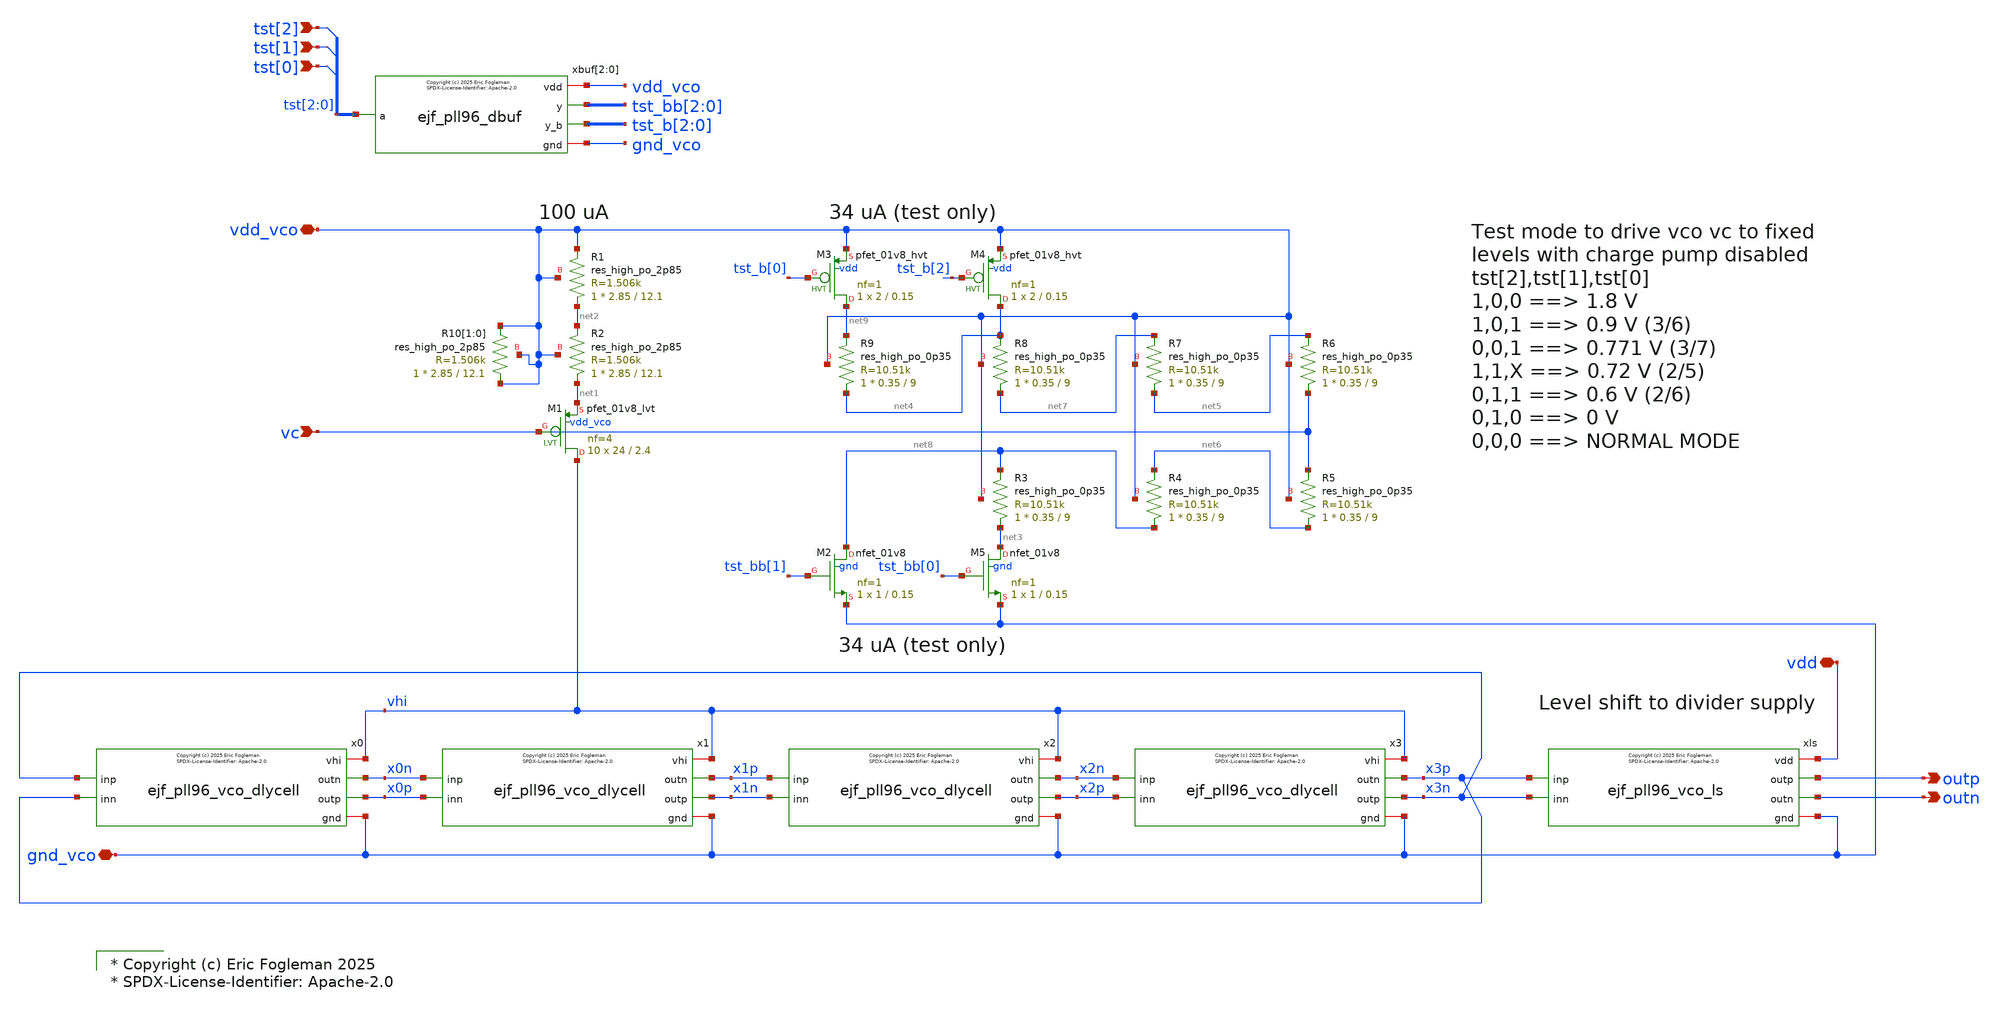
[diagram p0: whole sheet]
** sch_path: xschem/ejf_pll96_vco.sch
* xschem/ejf_pll96_dbuf.sym:
* Copyright (c) 2025 Eric Fogleman

* Copyright (c) Eric Fogleman 2025
* SPDX-License-Identifier: Apache-2.0

**.subckt ejf_pll96_vco vc vdd_vco outp gnd_vco vdd outn tst[2] tst[1] tst[0]
*.ipin vc
*.iopin vdd_vco
*.opin outp
*.iopin gnd_vco
*.iopin vdd
*.opin outn
*.ipin tst[2]
*.ipin tst[1]
*.ipin tst[0]
x1 vhi x1p x1n x0n x0p gnd_vco ejf_pll96_vco_dlycell
x2 vhi x2n x2p x1p x1n gnd_vco ejf_pll96_vco_dlycell
x0 vhi x0n x0p x3n x3p gnd_vco ejf_pll96_vco_dlycell
x3 vhi x3p x3n x2n x2p gnd_vco ejf_pll96_vco_dlycell
xls vdd x3p outp outn x3n gnd_vco ejf_pll96_vco_ls
XM1 vhi vc net1 vdd_vco sky130_fd_pr__pfet_01v8_lvt L=2.4 W=24 nf=4 ad='int((nf+1)/2) * W/nf * 0.29'
+ as='int((nf+2)/2) * W/nf * 0.29' pd='2*int((nf+1)/2) * (W/nf + 0.29)' ps='2*int((nf+2)/2) * (W/nf + 0.29)'
+ nrd='0.29 / W' nrs='0.29 / W' sa=0 sb=0 sd=0 mult=10 m=10
XR1 net2 vdd_vco vdd_vco sky130_fd_pr__res_high_po_2p85 L=12.1 mult=1 m=1
XR2 net1 net2 vdd_vco sky130_fd_pr__res_high_po_2p85 L=12.1 mult=1 m=1
XR10[1] vdd_vco vdd_vco vdd_vco sky130_fd_pr__res_high_po_2p85 L=12.1 mult=1 m=1
XR10[0] vdd_vco vdd_vco vdd_vco sky130_fd_pr__res_high_po_2p85 L=12.1 mult=1 m=1
XM2 net8 tst_bb[1] gnd_vco gnd sky130_fd_pr__nfet_01v8 L=0.15 W=1 nf=1 ad='int((nf+1)/2) * W/nf * 0.29'
+ as='int((nf+2)/2) * W/nf * 0.29' pd='2*int((nf+1)/2) * (W/nf + 0.29)' ps='2*int((nf+2)/2) * (W/nf + 0.29)'
+ nrd='0.29 / W' nrs='0.29 / W' sa=0 sb=0 sd=0 mult=1 m=1
XM3 net9 tst_b[0] vdd_vco vdd sky130_fd_pr__pfet_01v8_hvt L=0.15 W=2 nf=1 ad='int((nf+1)/2) * W/nf * 0.29'
+ as='int((nf+2)/2) * W/nf * 0.29' pd='2*int((nf+1)/2) * (W/nf + 0.29)' ps='2*int((nf+2)/2) * (W/nf + 0.29)'
+ nrd='0.29 / W' nrs='0.29 / W' sa=0 sb=0 sd=0 mult=1 m=1
XM4 net4 tst_b[2] vdd_vco vdd sky130_fd_pr__pfet_01v8_hvt L=0.15 W=2 nf=1 ad='int((nf+1)/2) * W/nf * 0.29'
+ as='int((nf+2)/2) * W/nf * 0.29' pd='2*int((nf+1)/2) * (W/nf + 0.29)' ps='2*int((nf+2)/2) * (W/nf + 0.29)'
+ nrd='0.29 / W' nrs='0.29 / W' sa=0 sb=0 sd=0 mult=1 m=1
XM5 net3 tst_bb[0] gnd_vco gnd sky130_fd_pr__nfet_01v8 L=0.15 W=1 nf=1 ad='int((nf+1)/2) * W/nf * 0.29'
+ as='int((nf+2)/2) * W/nf * 0.29' pd='2*int((nf+1)/2) * (W/nf + 0.29)' ps='2*int((nf+2)/2) * (W/nf + 0.29)'
+ nrd='0.29 / W' nrs='0.29 / W' sa=0 sb=0 sd=0 mult=1 m=1
xbuf[2] vdd_vco tst[2] tst_bb[2] tst_b[2] gnd_vco ejf_pll96_dbuf
xbuf[1] vdd_vco tst[1] tst_bb[1] tst_b[1] gnd_vco ejf_pll96_dbuf
xbuf[0] vdd_vco tst[0] tst_bb[0] tst_b[0] gnd_vco ejf_pll96_dbuf
XR4 net8 net6 vdd_vco sky130_fd_pr__res_high_po_0p35 L=9 mult=1 m=1
XR3 net3 net8 vdd_vco sky130_fd_pr__res_high_po_0p35 L=9 mult=1 m=1
XR5 net6 vc vdd_vco sky130_fd_pr__res_high_po_0p35 L=9 mult=1 m=1
XR6 vc net5 vdd_vco sky130_fd_pr__res_high_po_0p35 L=9 mult=1 m=1
XR7 net5 net7 vdd_vco sky130_fd_pr__res_high_po_0p35 L=9 mult=1 m=1
XR8 net7 net4 vdd_vco sky130_fd_pr__res_high_po_0p35 L=9 mult=1 m=1
XR9 net4 net9 vdd_vco sky130_fd_pr__res_high_po_0p35 L=9 mult=1 m=1
**.ends

* expanding   symbol:  ejf_pll96_vco_dlycell.sym # of pins=6
** sym_path: xschem/ejf_pll96_vco_dlycell.sym
** sch_path: xschem/ejf_pll96_vco_dlycell.sch
.subckt ejf_pll96_vco_dlycell vhi outn outp inp inn gnd
*.ipin inp
*.opin outn
*.ipin inn
*.opin outp
*.iopin vhi
*.iopin gnd
XM11 outp outn gnd gnd sky130_fd_pr__nfet_01v8 L=0.44 W=1.22 nf=1 ad='int((nf+1)/2) * W/nf * 0.29' as='int((nf+2)/2) * W/nf * 0.29'
+ pd='2*int((nf+1)/2) * (W/nf + 0.29)' ps='2*int((nf+2)/2) * (W/nf + 0.29)' nrd='0.29 / W' nrs='0.29 / W'
+ sa=0 sb=0 sd=0 mult=1 m=1
XM13 outn inp gnd gnd sky130_fd_pr__nfet_01v8 L=0.44 W=4.88 nf=4 ad='int((nf+1)/2) * W/nf * 0.29' as='int((nf+2)/2) * W/nf * 0.29'
+ pd='2*int((nf+1)/2) * (W/nf + 0.29)' ps='2*int((nf+2)/2) * (W/nf + 0.29)' nrd='0.29 / W' nrs='0.29 / W'
+ sa=0 sb=0 sd=0 mult=1 m=1
XM14 outn inp vhi vhi sky130_fd_pr__pfet_01v8_hvt L=0.44 W=19.44 nf=6 ad='int((nf+1)/2) * W/nf * 0.29'
+ as='int((nf+2)/2) * W/nf * 0.29' pd='2*int((nf+1)/2) * (W/nf + 0.29)' ps='2*int((nf+2)/2) * (W/nf + 0.29)'
+ nrd='0.29 / W' nrs='0.29 / W' sa=0 sb=0 sd=0 mult=1 m=1
XM27 outn outp gnd gnd sky130_fd_pr__nfet_01v8 L=0.44 W=1.22 nf=1 ad='int((nf+1)/2) * W/nf * 0.29' as='int((nf+2)/2) * W/nf * 0.29'
+ pd='2*int((nf+1)/2) * (W/nf + 0.29)' ps='2*int((nf+2)/2) * (W/nf + 0.29)' nrd='0.29 / W' nrs='0.29 / W'
+ sa=0 sb=0 sd=0 mult=1 m=1
XM31 outp inn gnd gnd sky130_fd_pr__nfet_01v8 L=0.44 W=4.88 nf=4 ad='int((nf+1)/2) * W/nf * 0.29' as='int((nf+2)/2) * W/nf * 0.29'
+ pd='2*int((nf+1)/2) * (W/nf + 0.29)' ps='2*int((nf+2)/2) * (W/nf + 0.29)' nrd='0.29 / W' nrs='0.29 / W'
+ sa=0 sb=0 sd=0 mult=1 m=1
XM30 outp inn vhi vhi sky130_fd_pr__pfet_01v8_hvt L=0.44 W=19.44 nf=6 ad='int((nf+1)/2) * W/nf * 0.29'
+ as='int((nf+2)/2) * W/nf * 0.29' pd='2*int((nf+1)/2) * (W/nf + 0.29)' ps='2*int((nf+2)/2) * (W/nf + 0.29)'
+ nrd='0.29 / W' nrs='0.29 / W' sa=0 sb=0 sd=0 mult=1 m=1
C3 inp gnd {CP} m=1
C4 inn gnd {CP} m=1
**** begin user architecture code

* Copyright (c) Eric Fogleman 2025
* SPDX-License-Identifier: Apache-2.0

**** end user architecture code
.ends


* expanding   symbol:  ejf_pll96_vco_ls.sym # of pins=6
** sym_path: xschem/ejf_pll96_vco_ls.sym
** sch_path: xschem/ejf_pll96_vco_ls.sch
.subckt ejf_pll96_vco_ls vdd inp outp outn inn gnd
*.ipin inp
*.opin outn
*.ipin inn
*.opin outp
*.iopin vdd
*.iopin gnd
XM5 net1 ls_outn vdd vdd sky130_fd_pr__pfet_01v8_hvt L=0.15 W=2 nf=1 ad='int((nf+1)/2) * W/nf * 0.29'
+ as='int((nf+2)/2) * W/nf * 0.29' pd='2*int((nf+1)/2) * (W/nf + 0.29)' ps='2*int((nf+2)/2) * (W/nf + 0.29)'
+ nrd='0.29 / W' nrs='0.29 / W' sa=0 sb=0 sd=0 mult=1 m=1
XM1 ls_outn inp gnd gnd sky130_fd_pr__nfet_01v8 L=0.15 W=2 nf=1 ad='int((nf+1)/2) * W/nf * 0.29' as='int((nf+2)/2) * W/nf * 0.29'
+ pd='2*int((nf+1)/2) * (W/nf + 0.29)' ps='2*int((nf+2)/2) * (W/nf + 0.29)' nrd='0.29 / W' nrs='0.29 / W'
+ sa=0 sb=0 sd=0 mult=1 m=1
XM2 ls_outp inn gnd gnd sky130_fd_pr__nfet_01v8 L=0.15 W=2 nf=1 ad='int((nf+1)/2) * W/nf * 0.29' as='int((nf+2)/2) * W/nf * 0.29'
+ pd='2*int((nf+1)/2) * (W/nf + 0.29)' ps='2*int((nf+2)/2) * (W/nf + 0.29)' nrd='0.29 / W' nrs='0.29 / W'
+ sa=0 sb=0 sd=0 mult=1 m=1
XM3 net2 ls_outp vdd vdd sky130_fd_pr__pfet_01v8_hvt L=0.15 W=2 nf=1 ad='int((nf+1)/2) * W/nf * 0.29'
+ as='int((nf+2)/2) * W/nf * 0.29' pd='2*int((nf+1)/2) * (W/nf + 0.29)' ps='2*int((nf+2)/2) * (W/nf + 0.29)'
+ nrd='0.29 / W' nrs='0.29 / W' sa=0 sb=0 sd=0 mult=1 m=1
XM4 ls_outn inp net2 vdd sky130_fd_pr__pfet_01v8_hvt L=0.15 W=2 nf=1 ad='int((nf+1)/2) * W/nf * 0.29'
+ as='int((nf+2)/2) * W/nf * 0.29' pd='2*int((nf+1)/2) * (W/nf + 0.29)' ps='2*int((nf+2)/2) * (W/nf + 0.29)'
+ nrd='0.29 / W' nrs='0.29 / W' sa=0 sb=0 sd=0 mult=1 m=1
XM6 ls_outp inn net1 vdd sky130_fd_pr__pfet_01v8_hvt L=0.15 W=2 nf=1 ad='int((nf+1)/2) * W/nf * 0.29'
+ as='int((nf+2)/2) * W/nf * 0.29' pd='2*int((nf+1)/2) * (W/nf + 0.29)' ps='2*int((nf+2)/2) * (W/nf + 0.29)'
+ nrd='0.29 / W' nrs='0.29 / W' sa=0 sb=0 sd=0 mult=1 m=1
XM7 outn ls_outp gnd gnd sky130_fd_pr__nfet_01v8 L=0.15 W=2 nf=1 ad='int((nf+1)/2) * W/nf * 0.29' as='int((nf+2)/2) * W/nf * 0.29'
+ pd='2*int((nf+1)/2) * (W/nf + 0.29)' ps='2*int((nf+2)/2) * (W/nf + 0.29)' nrd='0.29 / W' nrs='0.29 / W'
+ sa=0 sb=0 sd=0 mult=1 m=1
XM8 outn ls_outp vdd vdd sky130_fd_pr__pfet_01v8_hvt L=0.15 W=4 nf=1 ad='int((nf+1)/2) * W/nf * 0.29'
+ as='int((nf+2)/2) * W/nf * 0.29' pd='2*int((nf+1)/2) * (W/nf + 0.29)' ps='2*int((nf+2)/2) * (W/nf + 0.29)'
+ nrd='0.29 / W' nrs='0.29 / W' sa=0 sb=0 sd=0 mult=1 m=1
XM9 outp ls_outn gnd gnd sky130_fd_pr__nfet_01v8 L=0.15 W=2 nf=1 ad='int((nf+1)/2) * W/nf * 0.29' as='int((nf+2)/2) * W/nf * 0.29'
+ pd='2*int((nf+1)/2) * (W/nf + 0.29)' ps='2*int((nf+2)/2) * (W/nf + 0.29)' nrd='0.29 / W' nrs='0.29 / W'
+ sa=0 sb=0 sd=0 mult=1 m=1
XM10 outp ls_outn vdd vdd sky130_fd_pr__pfet_01v8_hvt L=0.15 W=4 nf=1 ad='int((nf+1)/2) * W/nf * 0.29'
+ as='int((nf+2)/2) * W/nf * 0.29' pd='2*int((nf+1)/2) * (W/nf + 0.29)' ps='2*int((nf+2)/2) * (W/nf + 0.29)'
+ nrd='0.29 / W' nrs='0.29 / W' sa=0 sb=0 sd=0 mult=1 m=1
**** begin user architecture code

* Copyright (c) Eric Fogleman 2025
* SPDX-License-Identifier: Apache-2.0

**** end user architecture code
.ends


* expanding   symbol:  ejf_pll96_dbuf.sym # of pins=5
** sym_path: xschem/ejf_pll96_dbuf.sym
** sch_path: xschem/ejf_pll96_dbuf.sch
.subckt ejf_pll96_dbuf vdd a y y_b gnd
*.ipin a
*.iopin vdd
*.iopin gnd
*.opin y
*.opin y_b
XMP1 y_b a vdd vdd sky130_fd_pr__pfet_01v8_hvt L=0.15 W=2 nf=1 ad='int((nf+1)/2) * W/nf * 0.29' as='int((nf+2)/2) * W/nf * 0.29'
+ pd='2*int((nf+1)/2) * (W/nf + 0.29)' ps='2*int((nf+2)/2) * (W/nf + 0.29)' nrd='0.29 / W' nrs='0.29 / W'
+ sa=0 sb=0 sd=0 mult=1 m=1
XMP3 y y_b vdd vdd sky130_fd_pr__pfet_01v8_hvt L=0.15 W=2 nf=1 ad='int((nf+1)/2) * W/nf * 0.29' as='int((nf+2)/2) * W/nf * 0.29'
+ pd='2*int((nf+1)/2) * (W/nf + 0.29)' ps='2*int((nf+2)/2) * (W/nf + 0.29)' nrd='0.29 / W' nrs='0.29 / W'
+ sa=0 sb=0 sd=0 mult=1 m=1
XMN4 y y_b gnd gnd sky130_fd_pr__nfet_01v8 L=0.15 W=1 nf=1 ad='int((nf+1)/2) * W/nf * 0.29' as='int((nf+2)/2) * W/nf * 0.29'
+ pd='2*int((nf+1)/2) * (W/nf + 0.29)' ps='2*int((nf+2)/2) * (W/nf + 0.29)' nrd='0.29 / W' nrs='0.29 / W'
+ sa=0 sb=0 sd=0 mult=1 m=1
XMN2 y_b a gnd gnd sky130_fd_pr__nfet_01v8 L=0.15 W=1 nf=1 ad='int((nf+1)/2) * W/nf * 0.29' as='int((nf+2)/2) * W/nf * 0.29'
+ pd='2*int((nf+1)/2) * (W/nf + 0.29)' ps='2*int((nf+2)/2) * (W/nf + 0.29)' nrd='0.29 / W' nrs='0.29 / W'
+ sa=0 sb=0 sd=0 mult=1 m=1
**** begin user architecture code

* Copyright (c) Eric Fogleman 2025
* SPDX-License-Identifier: Apache-2.0

**** end user architecture code
.ends

.end
